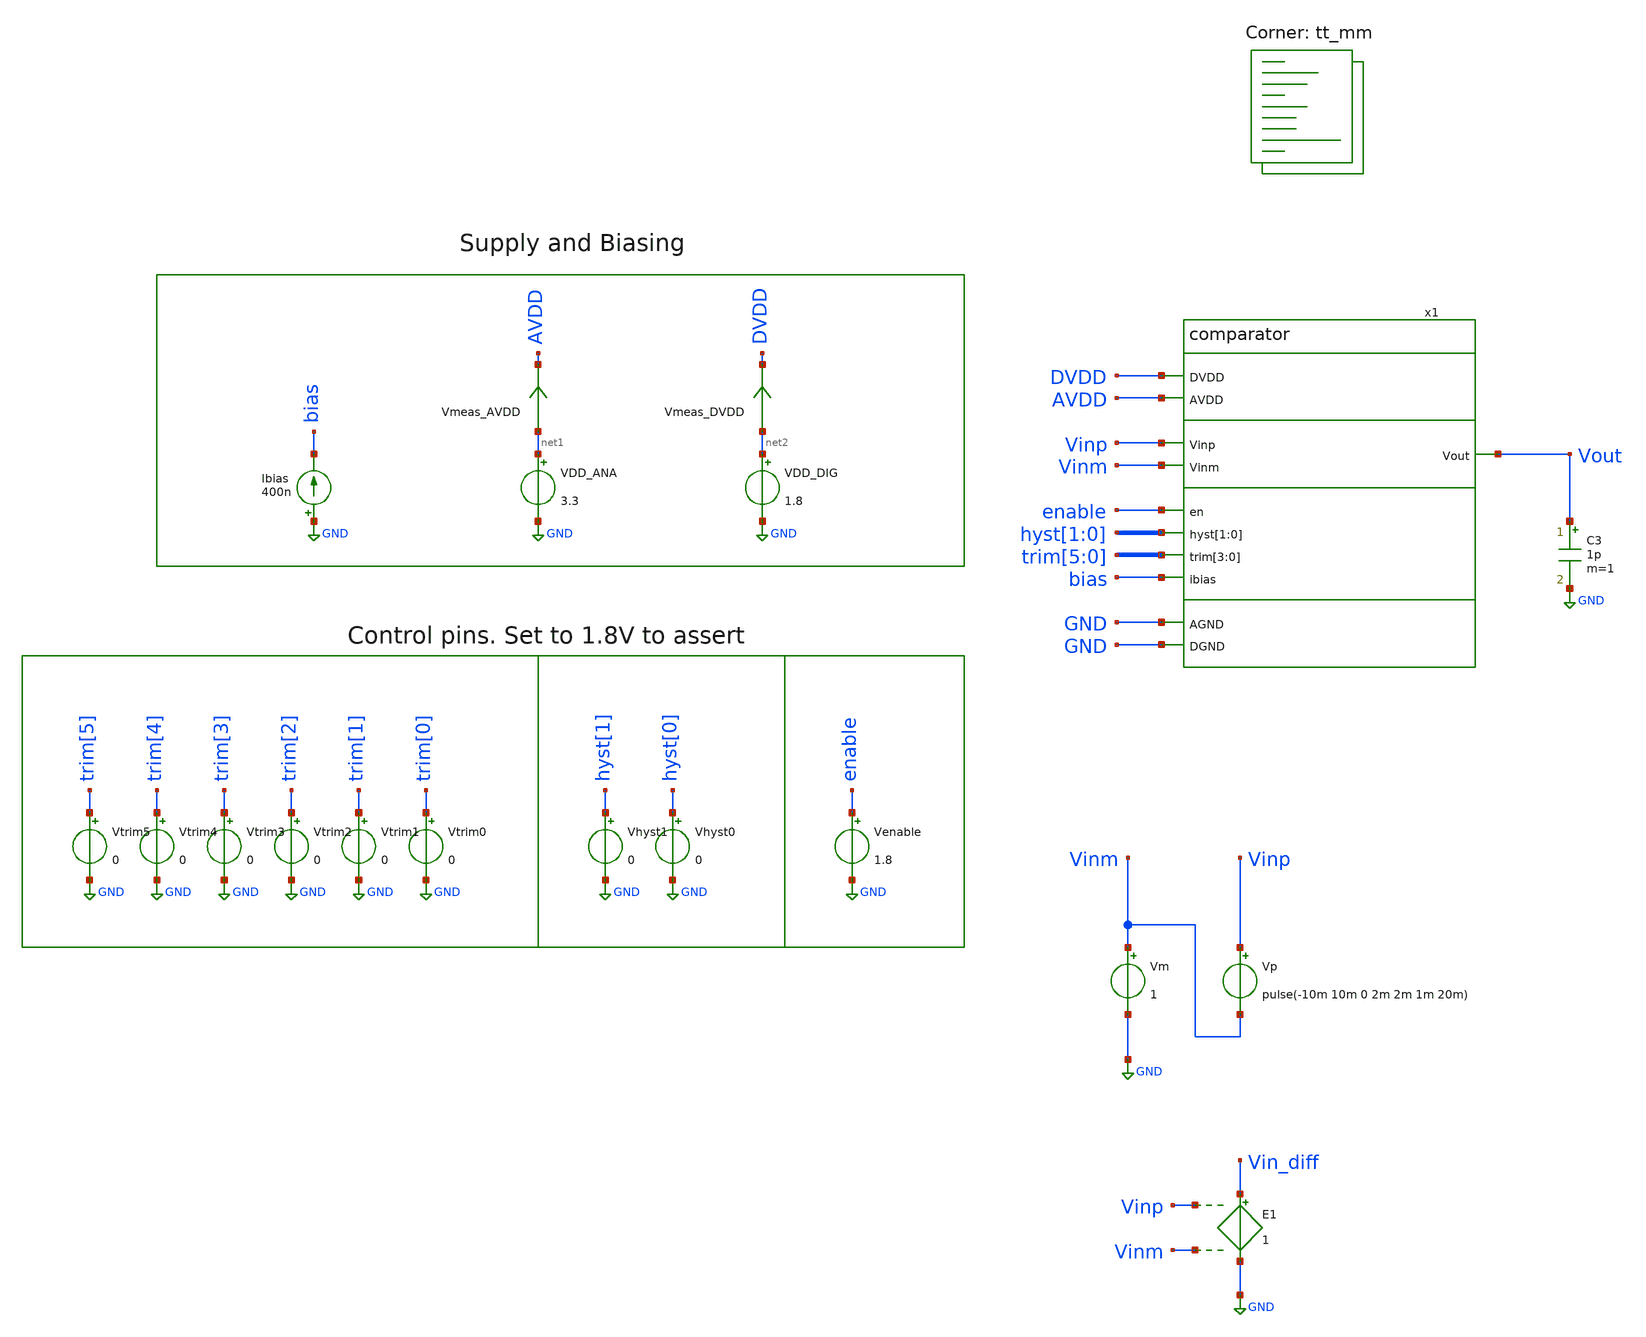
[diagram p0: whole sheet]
** sch_path: xschem/tb_comparator_offset_tran.sch
**.subckt tb_comparator_offset_tran
Vp Vinp Vinm pulse(-10m 10m 0 2m 2m 1m 20m)
VDD_ANA net1 GND 3.3
VDD_DIG net2 GND 1.8
Ibias GND bias 400n
C3 Vout GND 1p m=1
Vm Vinm GND 1
Vmeas_AVDD net1 AVDD 0
.save i(vmeas_avdd)
Vmeas_DVDD net2 DVDD 0
.save i(vmeas_dvdd)
E1 Vin_diff GND Vinp Vinm 1
Vtrim3 trim[3] GND 0
Vtrim2 trim[2] GND 0
Vtrim1 trim[1] GND 0
Vtrim0 trim[0] GND 0
Vhyst1 hyst[1] GND 0
Vhyst0 hyst[0] GND 0
Venable enable GND 1.8
Vtrim5 trim[5] GND 0
Vtrim4 trim[4] GND 0
x1 DVDD AVDD GND GND Vinp Vout Vinm enable hyst[1] hyst[0] trim[5] trim[4] trim[3] trim[2] bias
+ comparator
**** begin user architecture code
.lib $::SKYWATER_MODELS/sky130.lib.spice tt_mm


.save v(vout) v(vin_diff)
*.save all
.tran 1u 2m
.ic v(x1.vop)=0 v(x1.vdiff)=1.8 v(x1.vout_int)=0 v(x1.voutb)=1.8 v(vout)=0 v(x1.trim0_hv)=0
+  v(x1.trim1_hv)=0 v(x1.trim2_hv)=0 v(x1.trim3_hv)=0 v(x1.trim4_hv)=0 v(x1.trim5_hv)=0  v(x1.hyst1_hv)=0
+ v(x1.hyst0_hv)=0 v(x1.enb_hv)=0

.control
let vec=unitvec(1)
let num_meas = 5400
let num_meas_mini = 40
let input_offset = unitvec(num_meas)
let i = 0
let i_mini=0
foreach temp_val -40 25 85
   foreach vdd_ana_val 2.95 3.3 5.5
      foreach vm_val 0.02 {$vdd_ana_val/4} {$vdd_ana_val/2} {$vdd_ana_val*0.75} {-0.02+$vdd_ana_val}
         foreach ibias_val 388n 400n 412n
            let i_mini=0
            dowhile i_mini<num_meas_mini
               set temp=$temp_val
               alter VDD_ANA $vdd_ana_val
               alter Vm $vm_val
               alter ibias $ibias_val
               run
               print i
               echo temp: $temp_val
               echo VDDA: $vdd_ana_val
               echo Vinm: $vm_val
               echo Ibias: $ibias_val
               meas tran t_cross when v(vout)=0.9 rise=1
               meas tran in_cross find v(vin_diff) at=t_cross
               print vecmin(input_offset)
               print vecmax(input_offset)
               let input_offset[i] = in_cross
               let i = i+1
               let i_mini = i_mini+1
               set filetype=ascii
               set appendwrite
               set wr_singlescale
               setscale vec
               wrdata results_monte_carlo.out in_cross
               reset
            end
         end
      end
   end
end
*set filetype = ascii
*write results_monte_carlo.raw input_offset
print vecmin(input_offset)
print vecmax(input_offset)
.endc


**** end user architecture code
**.ends
.GLOBAL GND
.end
